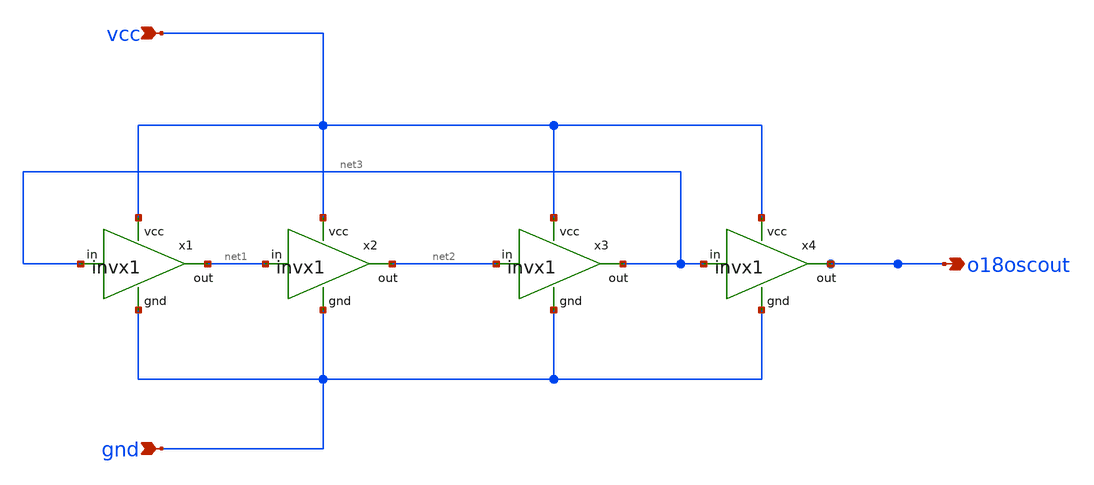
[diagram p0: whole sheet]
** sch_path: xschem/osu_soc_tsmc018/ringosc/ringosc.sch
**.subckt ringosc vcc gnd o18oscout
*.ipin vcc
*.ipin gnd
*.opin o18oscout
x1 vcc net3 net1 gnd invx1
x2 vcc net1 net2 gnd invx1
x3 vcc net2 net3 gnd invx1
x4 vcc net3 o18oscout gnd invx1
**.ends

* expanding   symbol:  ../inverter/invx1.sym # of pins=4
** sym_path: xschem/osu_soc_tsmc018/inverter/invx1.sym
** sch_path: xschem/osu_soc_tsmc018/inverter/invx1.sch
.subckt invx1 vcc in out gnd
*.ipin in
*.opin out
*.ipin vcc
*.ipin gnd
M1 out in vcc vcc pfet w=1u l=0.18u m=1
M2 out in gnd gnd nfet w=1u l=0.18u m=1
.ends

.end
